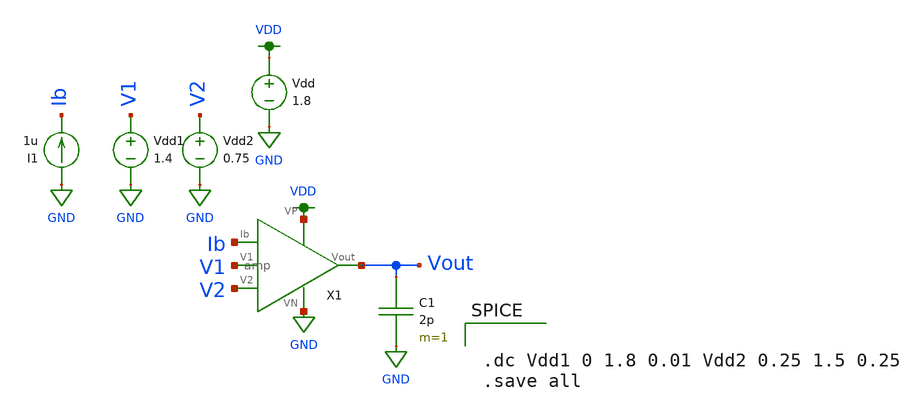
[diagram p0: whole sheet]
** sch_path: mp3/schematic/amp_tran.sch
**.subckt amp_tran
X1 Ib V1 V2 VDD GND Vout amp
Vdd1 V1 GND 1.4
Vdd2 V2 GND 0.75
I1 GND Ib 1u
Vdd VDD GND 1.8
C1 Vout GND 2p m=1
**** begin user architecture code

.option wnflag=1
.lib ~/skywater/skywater-pdk/libraries/sky130_fd_pr_ngspice/latest/models/sky130.lib.spice tt



.dc Vdd1 0 1.8 0.01 Vdd2 0.25 1.5 0.25
.save all

**** end user architecture code
**.ends

* expanding   symbol:  /home/madvlsi/madvlsi/mp3/schematic/amp.sym # of pins=6
** sym_path: mp3/schematic/amp.sym
** sch_path: mp3/schematic/amp.sch
.subckt amp Ib V1 V2 VP VN Vout
*.iopin VP
*.iopin VN
*.ipin Ib
*.opin Vout
*.ipin V1
*.ipin V2
X1 net1 net2 net3 net4 V1 V2 VP VN Vout fcda
X1 VP VN Ib net1 net2 net3 net4 bias
.ends


* expanding   symbol:  /home/madvlsi/madvlsi/mp3/schematic/fcda.sym # of pins=9
** sym_path: mp3/schematic/fcda.sym
** sch_path: mp3/schematic/fcda.sch
.subckt fcda Vcp Vcn Vbp Vbn V1 V2 VP VN Vout
*.iopin VP
*.iopin VN
*.ipin Vbp
*.ipin V2
*.ipin V1
*.ipin Vbn
*.ipin Vcp
*.ipin Vcn
*.opin Vout
XM100 net2 Vbp VP VDD sky130_fd_pr__pfet_01v8 L=0.5 W=12 nf=1 ad='int((nf+1)/2) * W/nf * 0.29' as='int((nf+2)/2) * W/nf * 0.29'
+ pd='2*int((nf+1)/2) * (W/nf + 0.29)' ps='2*int((nf+2)/2) * (W/nf + 0.29)' nrd='0.29 / W' nrs='0.29 / W'
+ sa=0 sb=0 sd=0 mult=1 m=1
XM21 net2 V1 net1 GND sky130_fd_pr__nfet_01v8 L=0.5 W=12 nf=1 ad='int((nf+1)/2) * W/nf * 0.29' as='int((nf+2)/2) * W/nf * 0.29'
+ pd='2*int((nf+1)/2) * (W/nf + 0.29)' ps='2*int((nf+2)/2) * (W/nf + 0.29)' nrd='0.29 / W' nrs='0.29 / W'
+ sa=0 sb=0 sd=0 mult=1 m=1
XM31 net3 V2 net1 GND sky130_fd_pr__nfet_01v8 L=0.5 W=12 nf=1 ad='int((nf+1)/2) * W/nf * 0.29' as='int((nf+2)/2) * W/nf * 0.29'
+ pd='2*int((nf+1)/2) * (W/nf + 0.29)' ps='2*int((nf+2)/2) * (W/nf + 0.29)' nrd='0.29 / W' nrs='0.29 / W'
+ sa=0 sb=0 sd=0 mult=1 m=1
XM41 net1 Vbn VN GND sky130_fd_pr__nfet_01v8 L=0.5 W=12 nf=1 ad='int((nf+1)/2) * W/nf * 0.29' as='int((nf+2)/2) * W/nf * 0.29'
+ pd='2*int((nf+1)/2) * (W/nf + 0.29)' ps='2*int((nf+2)/2) * (W/nf + 0.29)' nrd='0.29 / W' nrs='0.29 / W'
+ sa=0 sb=0 sd=0 mult=1 m=1
XM51 net3 Vbp VP VDD sky130_fd_pr__pfet_01v8 L=0.5 W=12 nf=1 ad='int((nf+1)/2) * W/nf * 0.29' as='int((nf+2)/2) * W/nf * 0.29'
+ pd='2*int((nf+1)/2) * (W/nf + 0.29)' ps='2*int((nf+2)/2) * (W/nf + 0.29)' nrd='0.29 / W' nrs='0.29 / W'
+ sa=0 sb=0 sd=0 mult=1 m=1
XM61 Vout Vcp net3 VDD sky130_fd_pr__pfet_01v8 L=0.5 W=12 nf=1 ad='int((nf+1)/2) * W/nf * 0.29' as='int((nf+2)/2) * W/nf * 0.29'
+ pd='2*int((nf+1)/2) * (W/nf + 0.29)' ps='2*int((nf+2)/2) * (W/nf + 0.29)' nrd='0.29 / W' nrs='0.29 / W'
+ sa=0 sb=0 sd=0 mult=1 m=1
XM71 net4 Vcp net2 VDD sky130_fd_pr__pfet_01v8 L=0.5 W=12 nf=1 ad='int((nf+1)/2) * W/nf * 0.29' as='int((nf+2)/2) * W/nf * 0.29'
+ pd='2*int((nf+1)/2) * (W/nf + 0.29)' ps='2*int((nf+2)/2) * (W/nf + 0.29)' nrd='0.29 / W' nrs='0.29 / W'
+ sa=0 sb=0 sd=0 mult=1 m=1
XM81 net4 Vcn net5 GND sky130_fd_pr__nfet_01v8 L=0.5 W=12 nf=1 ad='int((nf+1)/2) * W/nf * 0.29' as='int((nf+2)/2) * W/nf * 0.29'
+ pd='2*int((nf+1)/2) * (W/nf + 0.29)' ps='2*int((nf+2)/2) * (W/nf + 0.29)' nrd='0.29 / W' nrs='0.29 / W'
+ sa=0 sb=0 sd=0 mult=1 m=1
XM91 net6 net4 VN GND sky130_fd_pr__nfet_01v8 L=0.5 W=12 nf=1 ad='int((nf+1)/2) * W/nf * 0.29' as='int((nf+2)/2) * W/nf * 0.29'
+ pd='2*int((nf+1)/2) * (W/nf + 0.29)' ps='2*int((nf+2)/2) * (W/nf + 0.29)' nrd='0.29 / W' nrs='0.29 / W'
+ sa=0 sb=0 sd=0 mult=1 m=1
XM101 Vout Vcn net6 GND sky130_fd_pr__nfet_01v8 L=0.5 W=12 nf=1 ad='int((nf+1)/2) * W/nf * 0.29' as='int((nf+2)/2) * W/nf * 0.29'
+ pd='2*int((nf+1)/2) * (W/nf + 0.29)' ps='2*int((nf+2)/2) * (W/nf + 0.29)' nrd='0.29 / W' nrs='0.29 / W'
+ sa=0 sb=0 sd=0 mult=1 m=1
XM111 VN net4 net5 GND sky130_fd_pr__nfet_01v8 L=0.5 W=12 nf=1 ad='int((nf+1)/2) * W/nf * 0.29' as='int((nf+2)/2) * W/nf * 0.29'
+ pd='2*int((nf+1)/2) * (W/nf + 0.29)' ps='2*int((nf+2)/2) * (W/nf + 0.29)' nrd='0.29 / W' nrs='0.29 / W'
+ sa=0 sb=0 sd=0 mult=1 m=1
.ends


* expanding   symbol:  /home/madvlsi/madvlsi/mp3/schematic/bias.sym # of pins=7
** sym_path: mp3/schematic/bias.sym
** sch_path: mp3/schematic/bias.sch
.subckt bias VP VN Ib Vcp Vcn Vbp Vbn
*.iopin VP
*.iopin VN
*.opin Vcp
*.opin Vcn
*.opin Vbp
*.iopin Ib
*.opin Vbn
XM1 net3 Vbn VP VDD sky130_fd_pr__pfet_01v8 L=0.5 W=12 nf=1 ad='int((nf+1)/2) * W/nf * 0.29' as='int((nf+2)/2) * W/nf * 0.29'
+ pd='2*int((nf+1)/2) * (W/nf + 0.29)' ps='2*int((nf+2)/2) * (W/nf + 0.29)' nrd='0.29 / W' nrs='0.29 / W'
+ sa=0 sb=0 sd=0 mult=1 m=1
XM2 Vbn Vbn net3 VDD sky130_fd_pr__pfet_01v8 L=0.5 W=48 nf=1 ad='int((nf+1)/2) * W/nf * 0.29' as='int((nf+2)/2) * W/nf * 0.29'
+ pd='2*int((nf+1)/2) * (W/nf + 0.29)' ps='2*int((nf+2)/2) * (W/nf + 0.29)' nrd='0.29 / W' nrs='0.29 / W'
+ sa=0 sb=0 sd=0 mult=1 m=1
XM3 net3 Vcp Vcp VDD sky130_fd_pr__pfet_01v8 L=0.5 W=12 nf=1 ad='int((nf+1)/2) * W/nf * 0.29' as='int((nf+2)/2) * W/nf * 0.29'
+ pd='2*int((nf+1)/2) * (W/nf + 0.29)' ps='2*int((nf+2)/2) * (W/nf + 0.29)' nrd='0.29 / W' nrs='0.29 / W'
+ sa=0 sb=0 sd=0 mult=1 m=1
XM4 Vbn Ib VN GND sky130_fd_pr__nfet_01v8 L=2.5 W=12 nf=1 ad='int((nf+1)/2) * W/nf * 0.29' as='int((nf+2)/2) * W/nf * 0.29'
+ pd='2*int((nf+1)/2) * (W/nf + 0.29)' ps='2*int((nf+2)/2) * (W/nf + 0.29)' nrd='0.29 / W' nrs='0.29 / W'
+ sa=0 sb=0 sd=0 mult=1 m=1
XM5 Vcp Ib VN GND sky130_fd_pr__nfet_01v8 L=0.5 W=12 nf=1 ad='int((nf+1)/2) * W/nf * 0.29' as='int((nf+2)/2) * W/nf * 0.29'
+ pd='2*int((nf+1)/2) * (W/nf + 0.29)' ps='2*int((nf+2)/2) * (W/nf + 0.29)' nrd='0.29 / W' nrs='0.29 / W'
+ sa=0 sb=0 sd=0 mult=1 m=1
XM6 net4 Ib VN GND sky130_fd_pr__nfet_01v8 L=0.5 W=12 nf=1 ad='int((nf+1)/2) * W/nf * 0.29' as='int((nf+2)/2) * W/nf * 0.29'
+ pd='2*int((nf+1)/2) * (W/nf + 0.29)' ps='2*int((nf+2)/2) * (W/nf + 0.29)' nrd='0.29 / W' nrs='0.29 / W'
+ sa=0 sb=0 sd=0 mult=1 m=1
XM7 net1 Vbp VP VDD sky130_fd_pr__pfet_01v8 L=2.5 W=12 nf=1 ad='int((nf+1)/2) * W/nf * 0.29' as='int((nf+2)/2) * W/nf * 0.29'
+ pd='2*int((nf+1)/2) * (W/nf + 0.29)' ps='2*int((nf+2)/2) * (W/nf + 0.29)' nrd='0.29 / W' nrs='0.29 / W'
+ sa=0 sb=0 sd=0 mult=1 m=1
XM8 Vcn Vbp VP VDD sky130_fd_pr__pfet_01v8 L=0.5 W=12 nf=1 ad='int((nf+1)/2) * W/nf * 0.29' as='int((nf+2)/2) * W/nf * 0.29'
+ pd='2*int((nf+1)/2) * (W/nf + 0.29)' ps='2*int((nf+2)/2) * (W/nf + 0.29)' nrd='0.29 / W' nrs='0.29 / W'
+ sa=0 sb=0 sd=0 mult=1 m=1
XM9 net2 Vcn Vcn GND sky130_fd_pr__nfet_01v8 L=0.5 W=12 nf=1 ad='int((nf+1)/2) * W/nf * 0.29' as='int((nf+2)/2) * W/nf * 0.29'
+ pd='2*int((nf+1)/2) * (W/nf + 0.29)' ps='2*int((nf+2)/2) * (W/nf + 0.29)' nrd='0.29 / W' nrs='0.29 / W'
+ sa=0 sb=0 sd=0 mult=1 m=1
XM10 net2 net1 VN GND sky130_fd_pr__nfet_01v8 L=0.5 W=12 nf=1 ad='int((nf+1)/2) * W/nf * 0.29' as='int((nf+2)/2) * W/nf * 0.29'
+ pd='2*int((nf+1)/2) * (W/nf + 0.29)' ps='2*int((nf+2)/2) * (W/nf + 0.29)' nrd='0.29 / W' nrs='0.29 / W'
+ sa=0 sb=0 sd=0 mult=1 m=1
XM11 net1 net1 net2 GND sky130_fd_pr__nfet_01v8 L=0.5 W=48 nf=1 ad='int((nf+1)/2) * W/nf * 0.29' as='int((nf+2)/2) * W/nf * 0.29'
+ pd='2*int((nf+1)/2) * (W/nf + 0.29)' ps='2*int((nf+2)/2) * (W/nf + 0.29)' nrd='0.29 / W' nrs='0.29 / W'
+ sa=0 sb=0 sd=0 mult=1 m=1
XM12 VN Ib Ib GND sky130_fd_pr__nfet_01v8 L=0.5 W=12 nf=1 ad='int((nf+1)/2) * W/nf * 0.29' as='int((nf+2)/2) * W/nf * 0.29'
+ pd='2*int((nf+1)/2) * (W/nf + 0.29)' ps='2*int((nf+2)/2) * (W/nf + 0.29)' nrd='0.29 / W' nrs='0.29 / W'
+ sa=0 sb=0 sd=0 mult=1 m=1
XM13 net4 net4 Vbp VDD sky130_fd_pr__pfet_01v8 L=0.5 W=12 nf=1 ad='int((nf+1)/2) * W/nf * 0.29' as='int((nf+2)/2) * W/nf * 0.29'
+ pd='2*int((nf+1)/2) * (W/nf + 0.29)' ps='2*int((nf+2)/2) * (W/nf + 0.29)' nrd='0.29 / W' nrs='0.29 / W'
+ sa=0 sb=0 sd=0 mult=1 m=1
.ends

.GLOBAL GND
.GLOBAL VDD
.end
